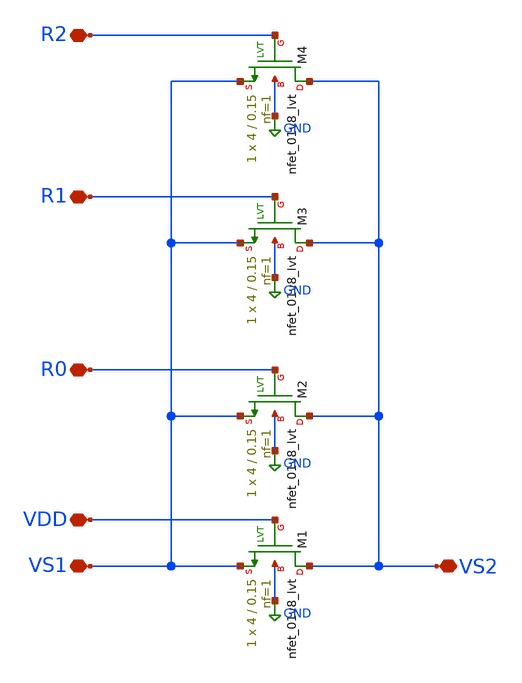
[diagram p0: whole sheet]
** sch_path: VGA/Rs_Banks.sch
**.subckt Rs_Banks R2 R1 R0 VDD VS1 VS2
*.iopin R2
*.iopin R1
*.iopin R0
*.iopin VDD
*.iopin VS1
*.iopin VS2
XM1 VS2 VDD VS1 GND sky130_fd_pr__nfet_01v8_lvt L=0.15 W=4 nf=1 ad='int((1 + 1)/2) * 4 / 1 * 0.29' as='int((1 + 2)/2) * 4 / 1 * 0.29'
+ pd='2*int((1 + 1)/2) * (4 / 1 + 0.29)' ps='2*int((1 + 2)/2) * (4 / 1 + 0.29)' nrd='0.29 / 4 ' nrs='0.29 / 4 '
+ sa=0 sb=0 sd=0 mult=1 m=1
XM2 VS2 R0 VS1 GND sky130_fd_pr__nfet_01v8_lvt L=0.15 W=4 nf=1 ad='int((1 + 1)/2) * 4 / 1 * 0.29' as='int((1 + 2)/2) * 4 / 1 * 0.29'
+ pd='2*int((1 + 1)/2) * (4 / 1 + 0.29)' ps='2*int((1 + 2)/2) * (4 / 1 + 0.29)' nrd='0.29 / 4 ' nrs='0.29 / 4 '
+ sa=0 sb=0 sd=0 mult=1 m=1
XM3 VS2 R1 VS1 GND sky130_fd_pr__nfet_01v8_lvt L=0.15 W=4 nf=1 ad='int((1 + 1)/2) * 4 / 1 * 0.29' as='int((1 + 2)/2) * 4 / 1 * 0.29'
+ pd='2*int((1 + 1)/2) * (4 / 1 + 0.29)' ps='2*int((1 + 2)/2) * (4 / 1 + 0.29)' nrd='0.29 / 4 ' nrs='0.29 / 4 '
+ sa=0 sb=0 sd=0 mult=1 m=1
XM4 VS2 R2 VS1 GND sky130_fd_pr__nfet_01v8_lvt L=0.15 W=4 nf=1 ad='int((1 + 1)/2) * 4 / 1 * 0.29' as='int((1 + 2)/2) * 4 / 1 * 0.29'
+ pd='2*int((1 + 1)/2) * (4 / 1 + 0.29)' ps='2*int((1 + 2)/2) * (4 / 1 + 0.29)' nrd='0.29 / 4 ' nrs='0.29 / 4 '
+ sa=0 sb=0 sd=0 mult=1 m=1
**.ends
.GLOBAL GND
.end
